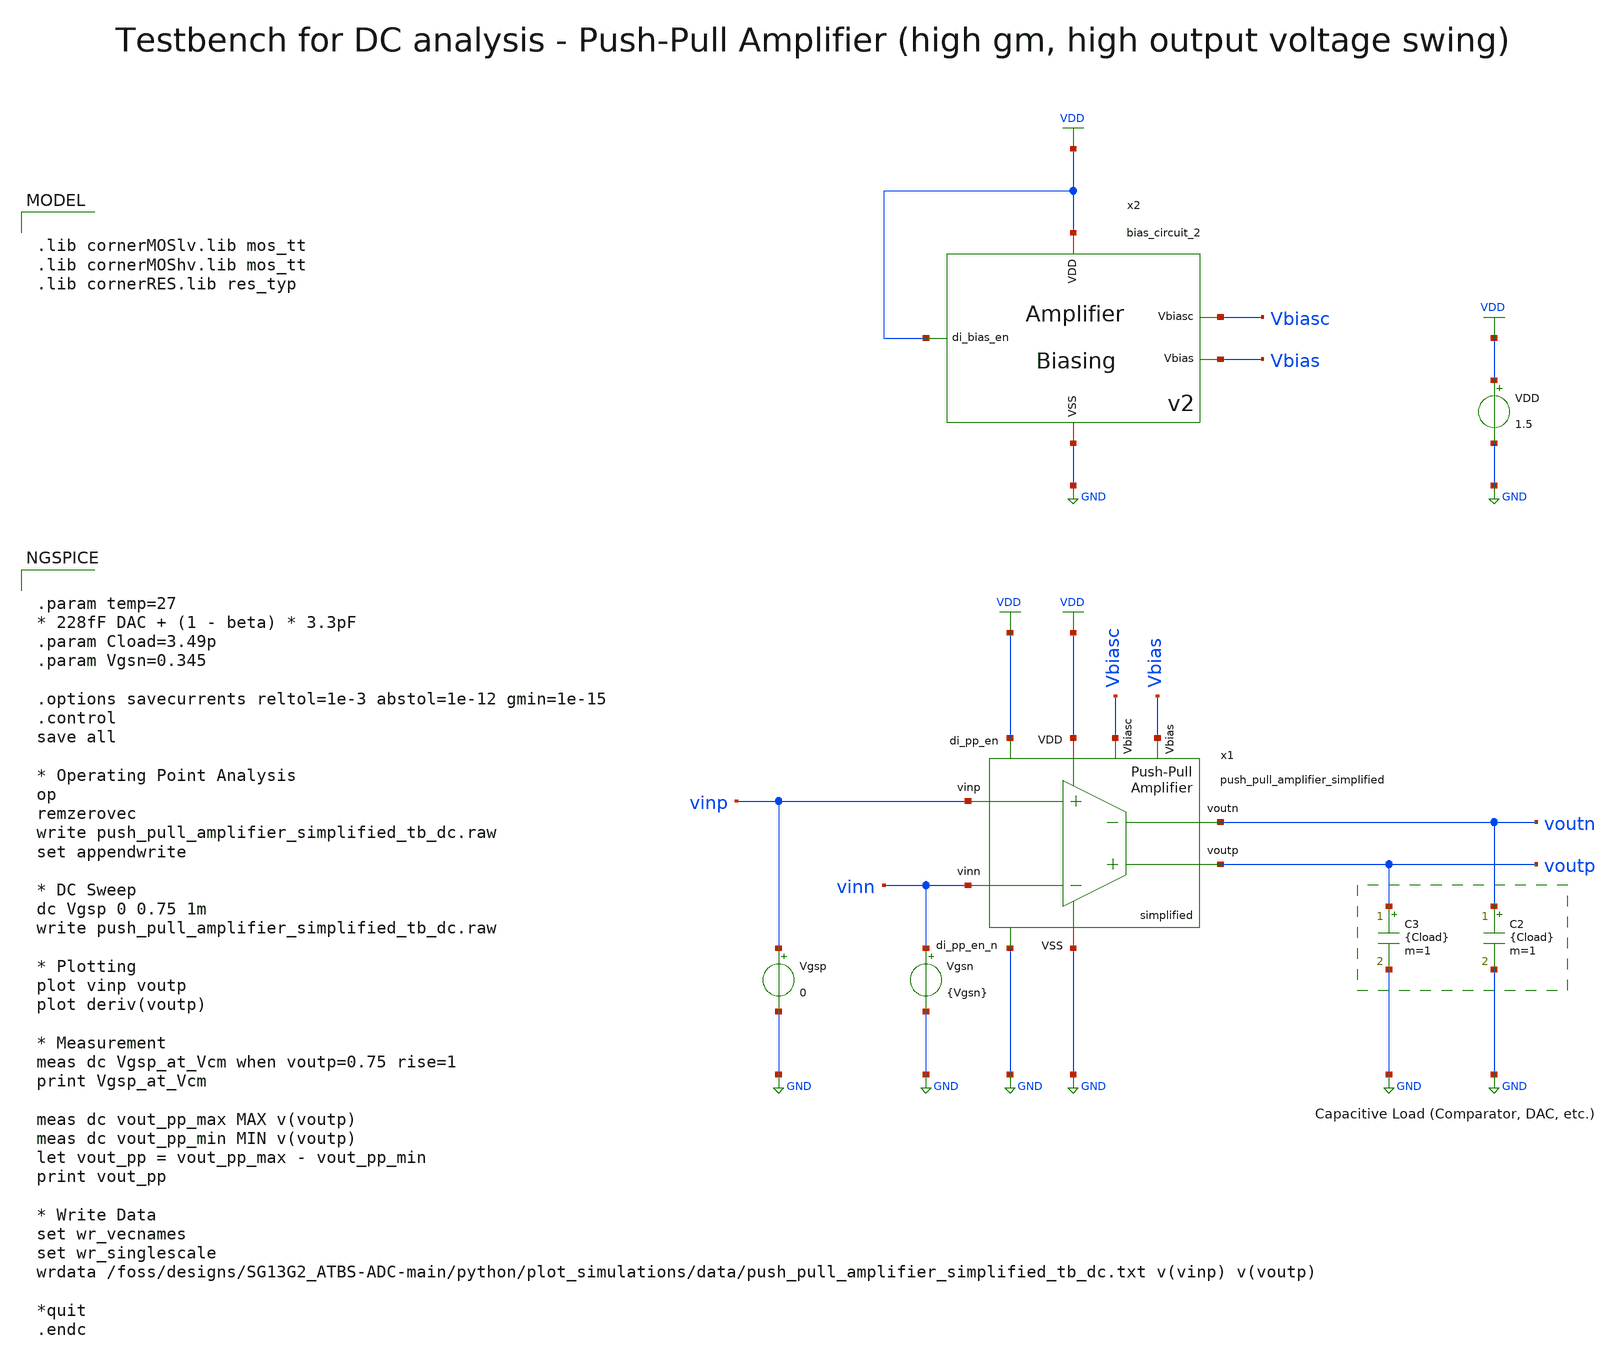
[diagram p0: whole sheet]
** sch_path: SG13G2_ATBS-ADC-main/xschem/bio_amplifier/amplifier_core/push_pull_amplifier/testbenches/push_pull_amplifier_simplified_tb_dc.sch
**.subckt push_pull_amplifier_simplified_tb_dc
VDD VDD GND 1.5
Vgsp vinp GND 0
C2 voutn GND {Cload} m=1
C3 voutp GND {Cload} m=1
Vgsn vinn GND {Vgsn}
x1 VDD voutp voutn vinn vinp GND GND VDD Vbiasc Vbias push_pull_amplifier_simplified
x2 VDD Vbiasc VDD GND Vbias bias_circuit_2
**** begin user architecture code


.param temp=27
* 228fF DAC + (1 - beta) * 3.3pF
.param Cload=3.49p
.param Vgsn=0.345

.options savecurrents reltol=1e-3 abstol=1e-12 gmin=1e-15
.control
save all

* Operating Point Analysis
op
remzerovec
write push_pull_amplifier_simplified_tb_dc.raw
set appendwrite

* DC Sweep
dc Vgsp 0 0.75 1m
write push_pull_amplifier_simplified_tb_dc.raw

* Plotting
plot vinp voutp
plot deriv(voutp)

* Measurement
meas dc Vgsp_at_Vcm when voutp=0.75 rise=1
print Vgsp_at_Vcm

meas dc vout_pp_max MAX v(voutp)
meas dc vout_pp_min MIN v(voutp)
let vout_pp = vout_pp_max - vout_pp_min
print vout_pp

* Write Data
set wr_vecnames
set wr_singlescale
wrdata
+ /foss/designs/SG13G2_ATBS-ADC-main/python/plot_simulations/data/push_pull_amplifier_simplified_tb_dc.txt v(vinp) v(voutp)

*quit
.endc



.lib cornerMOSlv.lib mos_tt
.lib cornerMOShv.lib mos_tt
.lib cornerRES.lib res_typ

**** end user architecture code
**.ends
.GLOBAL GND
.GLOBAL VDD
.end
